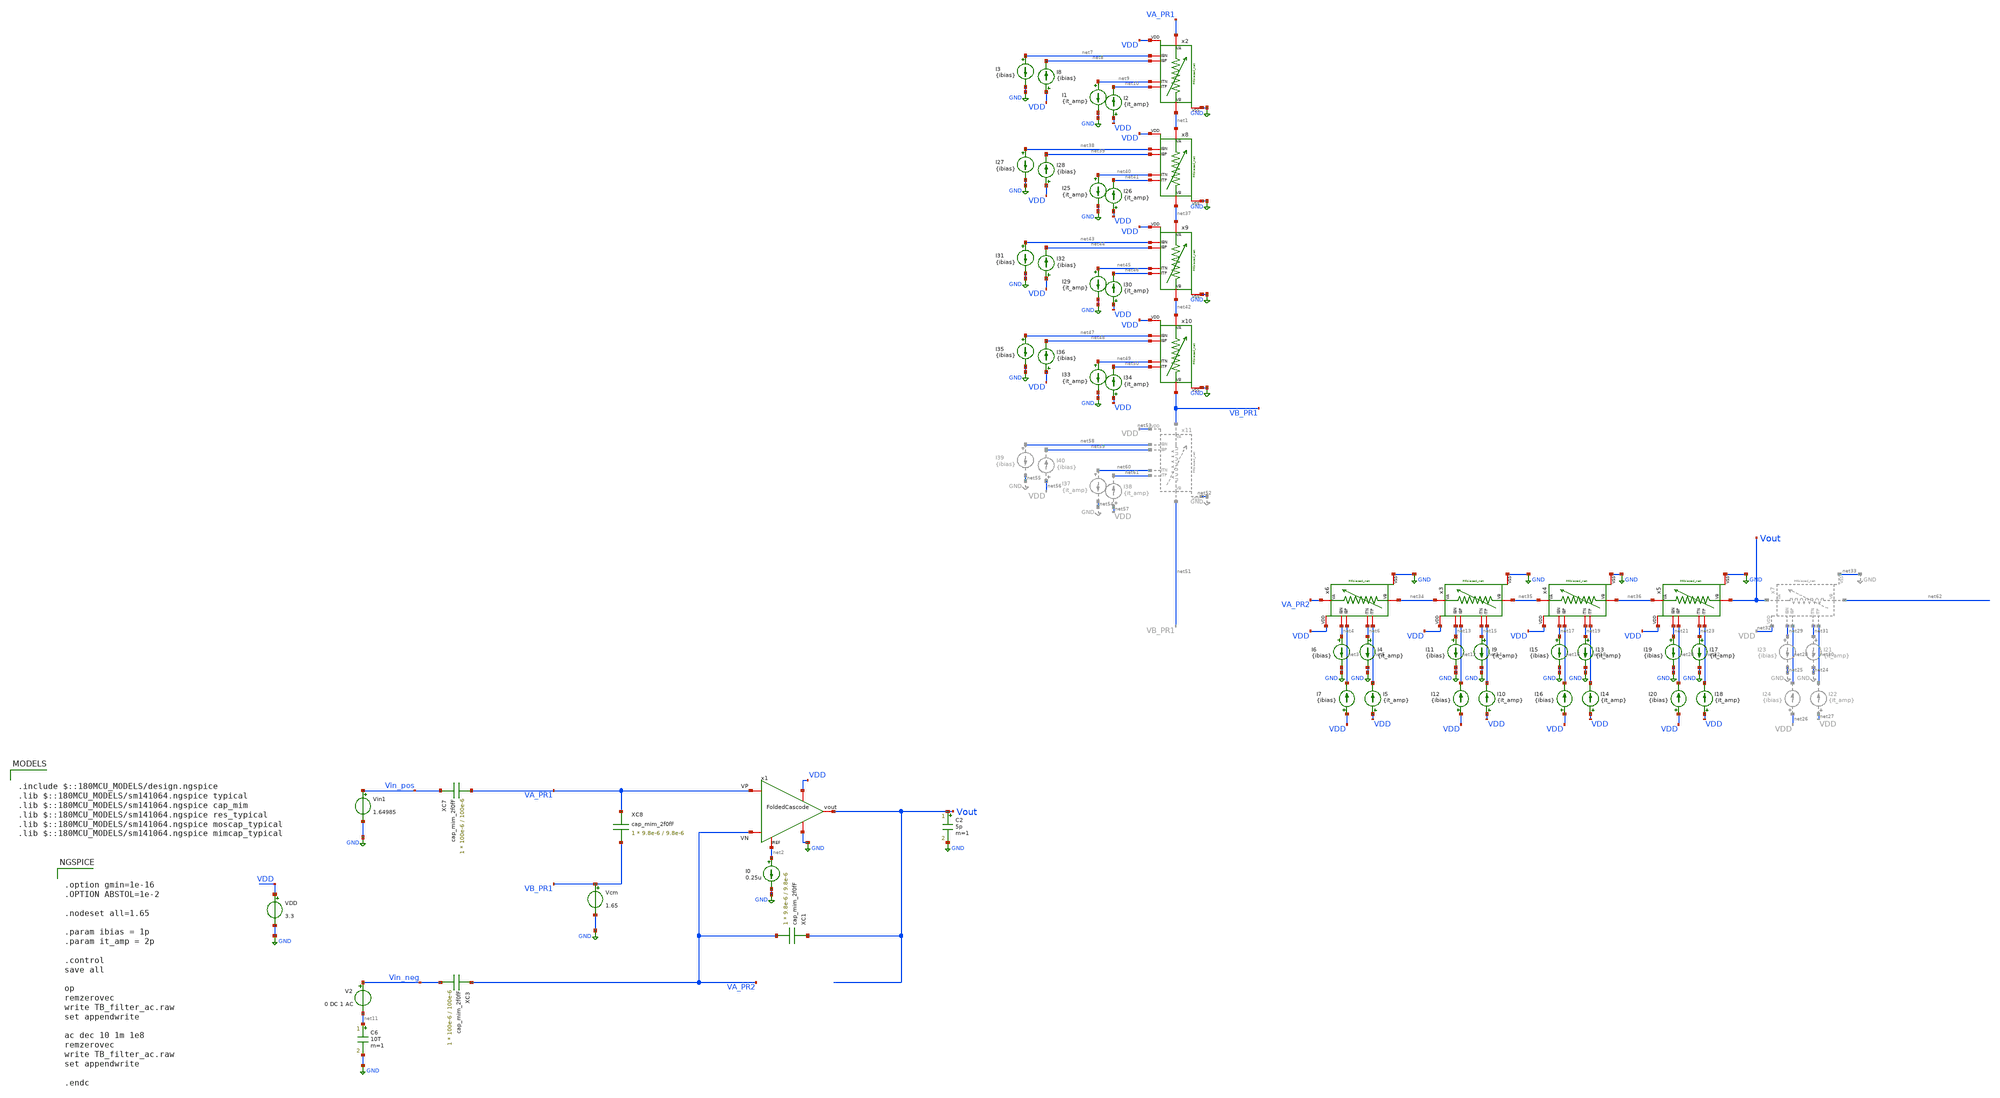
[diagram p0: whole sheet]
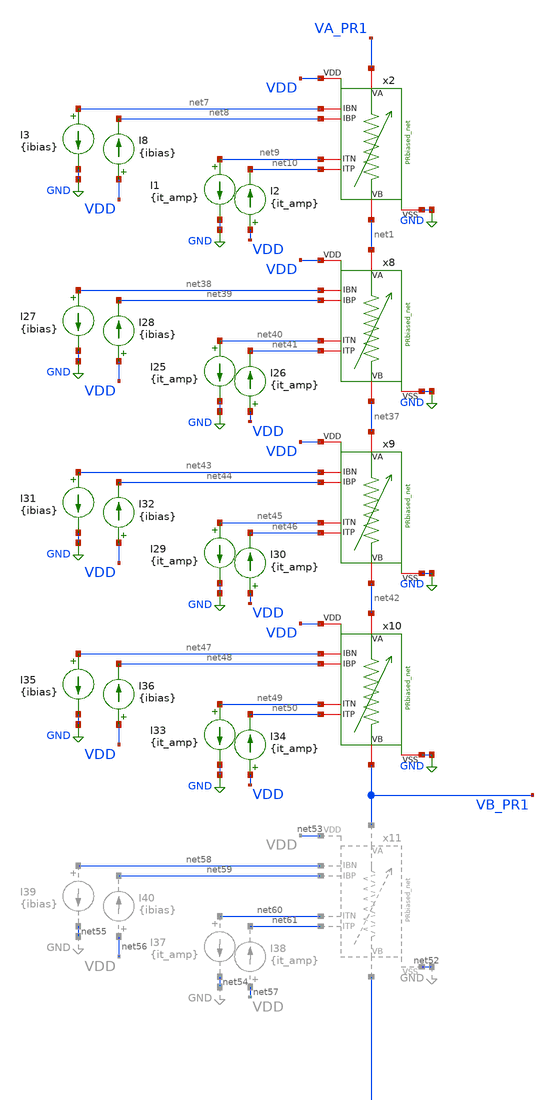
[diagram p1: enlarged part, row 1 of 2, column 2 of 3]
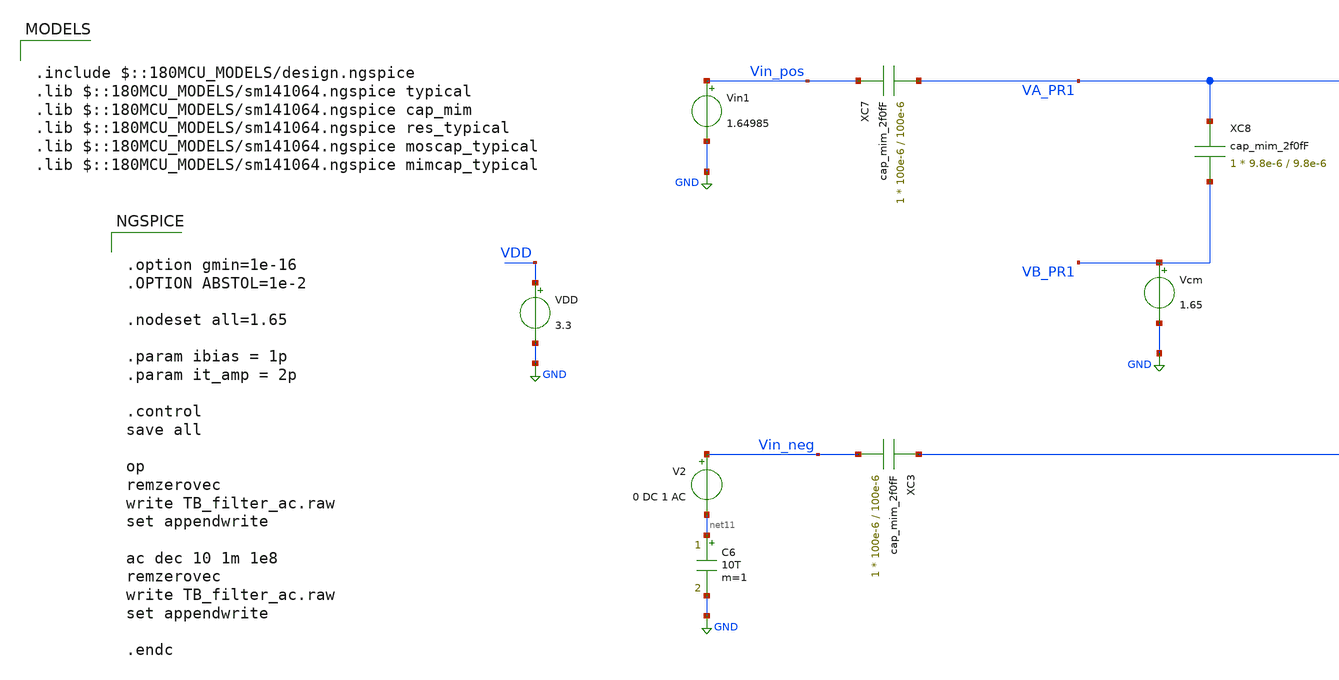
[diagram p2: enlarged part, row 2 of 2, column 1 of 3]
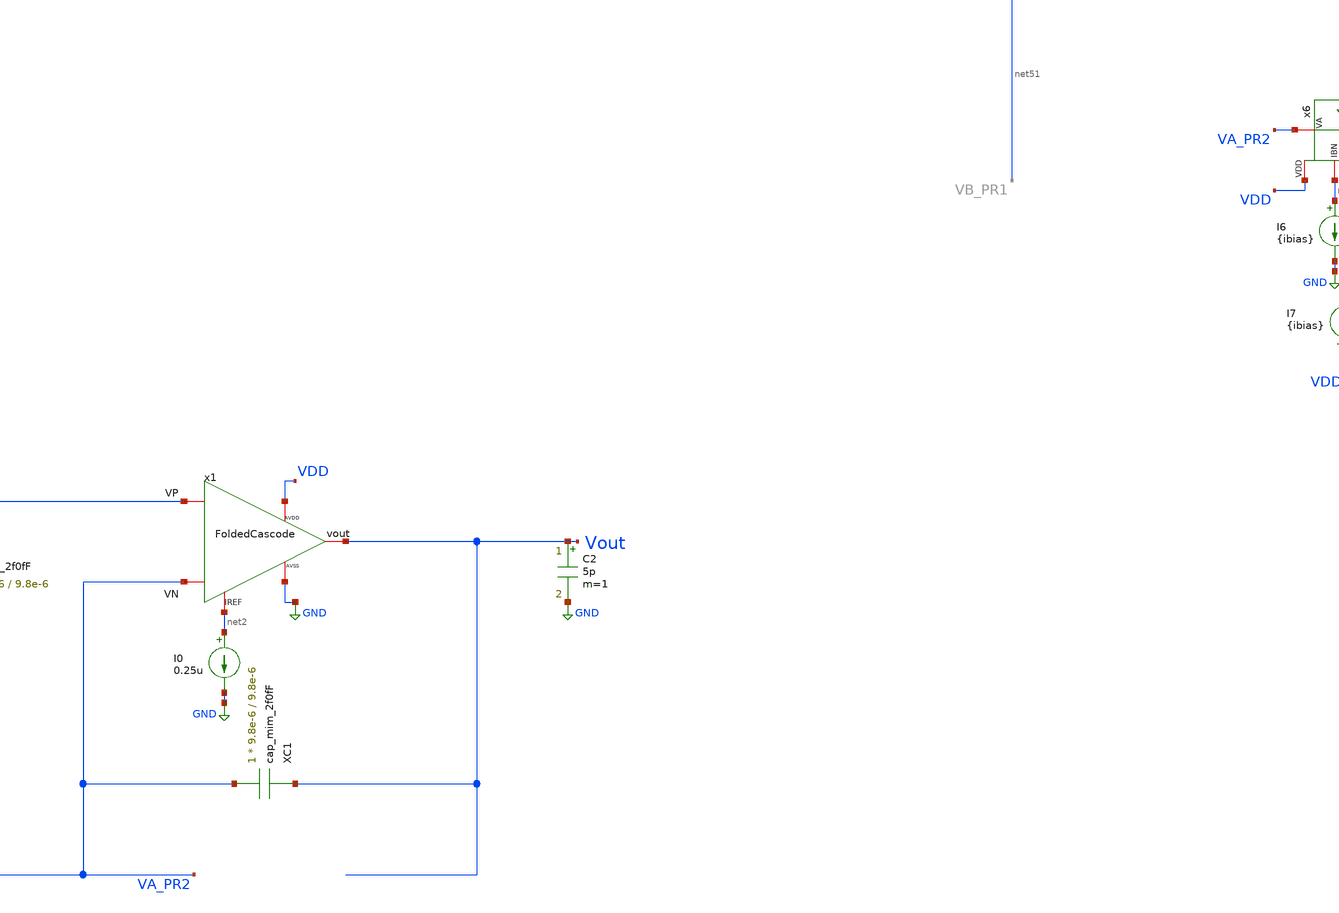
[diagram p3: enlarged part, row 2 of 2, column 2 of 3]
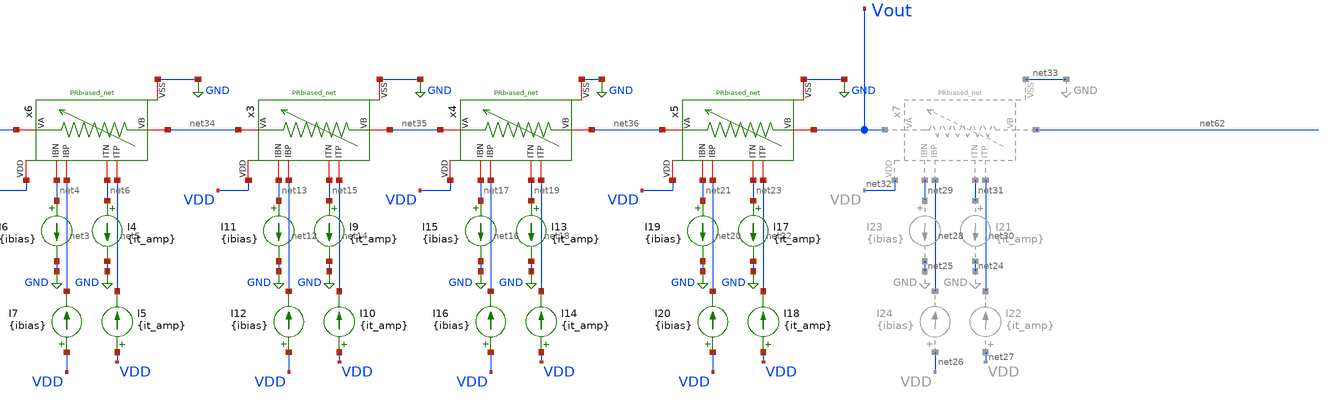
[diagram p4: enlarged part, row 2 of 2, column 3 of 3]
** sch_path: TIA_Filter/TB_filter_ac.sch
**.subckt TB_filter_ac
VDD VDD GND 3.3
C2 Vout GND 5p m=1
x1 VA_PR1 VA_PR2 Vout net2 VDD GND FoldedCascode
x6 VA_PR2 net34 net4 net3 net6 net5 VDD GND PRbiased_net
x2 VA_PR1 net1 net7 net8 net9 net10 VDD GND PRbiased_net
I0 net2 GND 0.25u
I4 net6 GND {it_amp}
I5 VDD net5 {it_amp}
I6 net4 GND {ibias}
I7 VDD net3 {ibias}
Vcm VB_PR1 GND 1.65
I1 net9 GND {it_amp}
I2 VDD net10 {it_amp}
I3 net7 GND {ibias}
I8 VDD net8 {ibias}
Vin1 Vin_pos GND 1.64985
V2 Vin_neg net11 0 DC 1 AC
C6 net11 GND 10T m=1
x3 net34 net35 net13 net12 net15 net14 VDD GND PRbiased_net
I9 net15 GND {it_amp}
I10 VDD net14 {it_amp}
I11 net13 GND {ibias}
I12 VDD net12 {ibias}
x4 net35 net36 net17 net16 net19 net18 VDD GND PRbiased_net
I13 net19 GND {it_amp}
I14 VDD net18 {it_amp}
I15 net17 GND {ibias}
I16 VDD net16 {ibias}
x5 net36 Vout net21 net20 net23 net22 VDD GND PRbiased_net
I17 net23 GND {it_amp}
I18 VDD net22 {it_amp}
I19 net21 GND {ibias}
I20 VDD net20 {ibias}
x8 net1 net37 net38 net39 net40 net41 VDD GND PRbiased_net
I25 net40 GND {it_amp}
I26 VDD net41 {it_amp}
I27 net38 GND {ibias}
I28 VDD net39 {ibias}
x9 net37 net42 net43 net44 net45 net46 VDD GND PRbiased_net
I29 net45 GND {it_amp}
I30 VDD net46 {it_amp}
I31 net43 GND {ibias}
I32 VDD net44 {ibias}
x10 net42 VB_PR1 net47 net48 net49 net50 VDD GND PRbiased_net
I33 net49 GND {it_amp}
I34 VDD net50 {it_amp}
I35 net47 GND {ibias}
I36 VDD net48 {ibias}
XC7 Vin_pos VA_PR1 cap_mim_2f0fF c_width=100e-6 c_length=100e-6 m=1
XC8 VA_PR1 VB_PR1 cap_mim_2f0fF c_width=9.8e-6 c_length=9.8e-6 m=1
XC1 Vout VA_PR2 cap_mim_2f0fF c_width=9.8e-6 c_length=9.8e-6 m=1
XC3 VA_PR2 Vin_neg cap_mim_2f0fF c_width=100e-6 c_length=100e-6 m=1
**** begin user architecture code

.include $::180MCU_MODELS/design.ngspice
.lib $::180MCU_MODELS/sm141064.ngspice typical
.lib $::180MCU_MODELS/sm141064.ngspice cap_mim
.lib $::180MCU_MODELS/sm141064.ngspice res_typical
.lib $::180MCU_MODELS/sm141064.ngspice moscap_typical
.lib $::180MCU_MODELS/sm141064.ngspice mimcap_typical



.option gmin=1e-16
.OPTION ABSTOL=1e-2

.nodeset all=1.65

.param ibias = 1p
.param it_amp = 2p

.control
save all

op
remzerovec
write TB_filter_ac.raw
set appendwrite

ac dec 10 1m 1e8
remzerovec
write TB_filter_ac.raw
set appendwrite

.endc


**** end user architecture code
**.ends
.GLOBAL GND
.end
